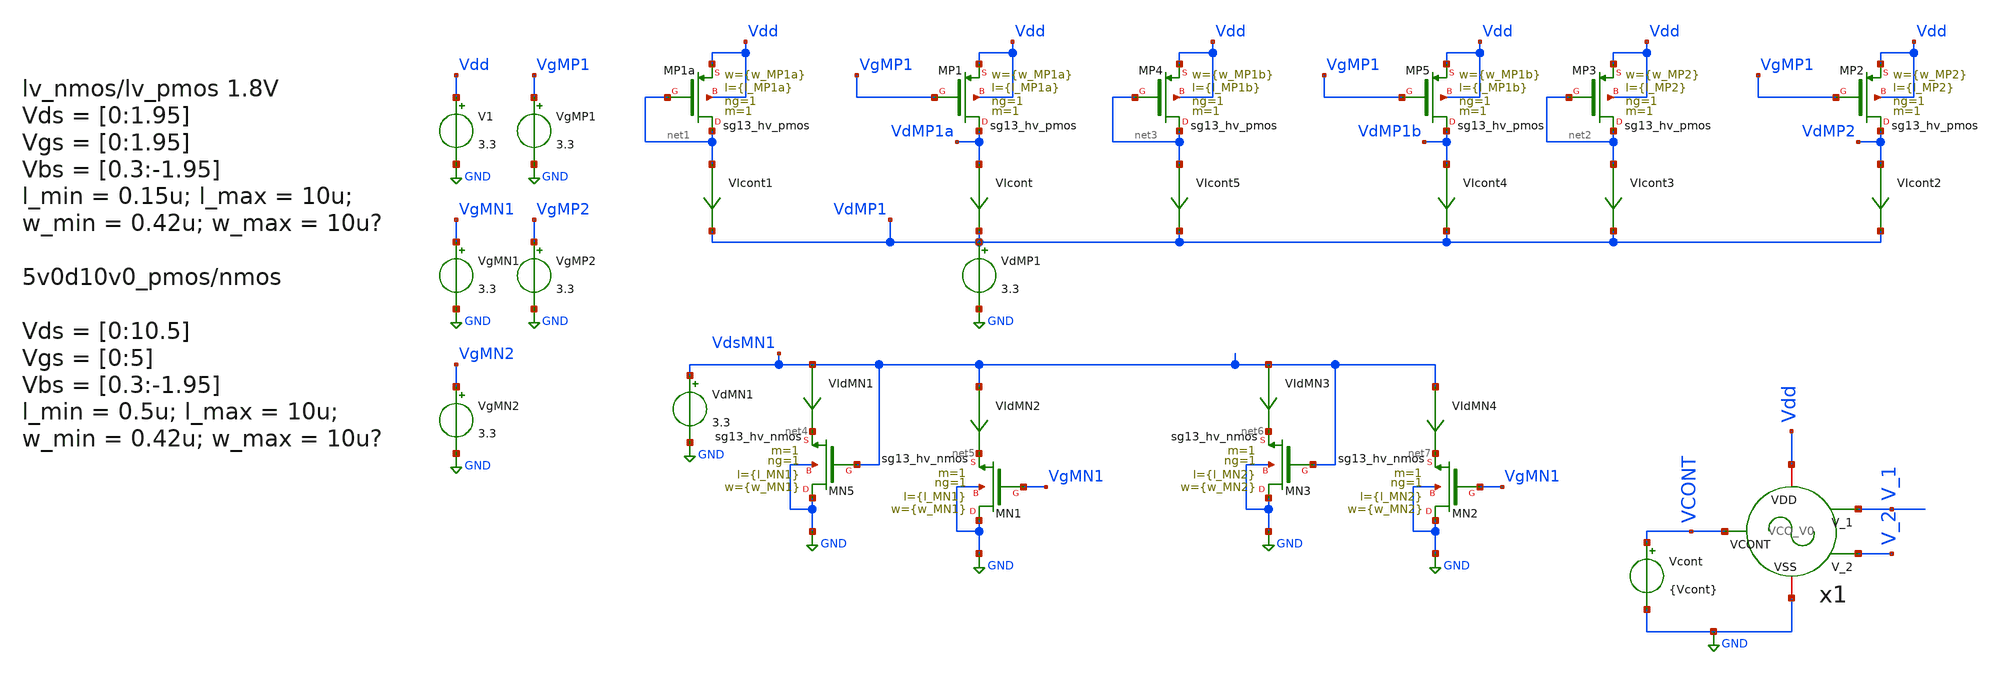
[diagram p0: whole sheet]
** sch_path: xschem/VCO/TB_VCO_Design_V0.sch
**.subckt TB_VCO_Design_V0
V1 Vdd GND 3.3
VIcont VdMP1a VdMP1 0
.save i(vicont)
VdMP1 VdMP1 GND 3.3
VgMP1 VgMP1 GND 3.3
VdMN1 VdsMN1 GND 3.3
VIdMN1 VdsMN1 net4 0
.save i(vidmn1)
VIcont1 net1 VdMP1 0
.save i(vicont1)
VIdMN2 VdsMN1 net5 0
.save i(vidmn2)
VgMN1 VgMN1 GND 3.3
VIdMN3 VdsMN1 net6 0
.save i(vidmn3)
VIdMN4 VdsMN1 net7 0
.save i(vidmn4)
VIcont2 VdMP2 VdMP1 0
.save i(vicont2)
VIcont3 net2 VdMP1 0
.save i(vicont3)
VgMP2 VgMP2 GND 3.3
VgMN2 VgMN2 GND 3.3
Vcont VCONT GND {Vcont}
x1 VCONT GND Vdd V_1 V_2 VCO_V0
XMP1a net1 net1 Vdd Vdd sg13_hv_pmos w={w_MP1a} l={l_MP1a} ng=1 m=1 mm_ok=1
XMP1 VdMP1a VgMP1 Vdd Vdd sg13_hv_pmos w={w_MP1a} l={l_MP1a} ng=1 m=1 mm_ok=1
XMP3 net2 net2 Vdd Vdd sg13_hv_pmos w={w_MP2} l={l_MP2} ng=1 m=1 mm_ok=1
XMP2 VdMP2 VgMP1 Vdd Vdd sg13_hv_pmos w={w_MP2} l={l_MP2} ng=1 m=1 mm_ok=1
XMN5 GND VdsMN1 net4 GND sg13_hv_nmos w={w_MN1} l={l_MN1} ng=1 m=1 mm_ok=1
XMN1 GND VgMN1 net5 GND sg13_hv_nmos w={w_MN1} l={l_MN1} ng=1 m=1 mm_ok=1
XMN3 GND VdsMN1 net6 GND sg13_hv_nmos w={w_MN2} l={l_MN2} ng=1 m=1 mm_ok=1
XMN2 GND VgMN1 net7 GND sg13_hv_nmos w={w_MN2} l={l_MN2} ng=1 m=1 mm_ok=1
VIcont4 VdMP1b VdMP1 0
.save i(vicont4)
VIcont5 net3 VdMP1 0
.save i(vicont5)
XMP4 net3 net3 Vdd Vdd sg13_hv_pmos w={w_MP1b} l={l_MP1b} ng=1 m=1 mm_ok=1
XMP5 VdMP1b VgMP1 Vdd Vdd sg13_hv_pmos w={w_MP1b} l={l_MP1b} ng=1 m=1 mm_ok=1
**** begin user architecture code


.save all


.csparam start = 10
.param Vcont = 1

.control

dc VdMP1 0 3.3 0.2 VgMP1 0 3.3 0.2
let IdMP1a = i(VIcont)
let IdMP1a_Diode = i(VIcont1)
let  VsdMP1 = v(Vdd) - v(VdMP1)
let VthMP1 = @n.xMP1.msky130_fd_pr__pfet_01v8[vth]
let  VovMP1a = v(Vdd) - v(VdMP1) - VthMP1
plot IdMP1a IdMP1a_Diode vs VsdMP1
plot IdMP1a_Diode vs VovMP1

let IdMP1b = i(VIcont4)
let IdMP1b_Diode = i(VIcont5)
let  VsdMP1 = v(Vdd) - v(VdMP1)
let VthMP1 = @n.xMP1.msky130_fd_pr__pfet_01v8[vth]
let  VovMP1b = v(Vdd) - v(VdMP1) - VthMP1
plot IdMP1b IdMP1b_Diode vs VsdMP1
plot IdMP1b_Diode vs VovMP1

let IdMP2 = i(VIcont2)
let IdMP2_Diode = i(VIcont3)
let  VsdMP2 = v(Vdd) - v(VdMP2)
let VthMP2 = @m.xMP4.msky130_fd_pr__pfet_01v8[vth]
let  VovMP2 = v(Vdd) - v(VdMP2) - VthMP2
*plot IdMP2 IdMP2_Diode vs VsdMP2
*plot IdMP2_Diode vs VovMP2
let KP1 = IdMP1_Diode/(VovMP1*VovMP1)
let AP1 = sqrt(KP1)
let KP2 = IdMP2_Diode/(VovMP2*VovMP2)
let AP2 = sqrt(KP2)

plot AP1 AP2

*plot IdMP1_Diode IdMP2_Diode vs VsdMP1
print VthMP1 VthMP2
*wrdata ../../sim_data/data_VCO_design.txt IdMP1_Diode VovMP1 IdMP1 vs VsdMP1
wrdata
+ /workspaces/usm-vlsi-tools/shared_xserver/simulations/SKY130/IPD500-TimebasedDCDCBuck/sim_data/data_VCO_design.txt IdMP1_Diode VovMP1 IdMP1 vs VsdMP1
wrdata
+ /workspaces/usm-vlsi-tools/shared_xserver/simulations/SKY130/IPD500-TimebasedDCDCBuck/sim_data/data_AP1_VthMP1.txt AP1 VthMP1 AP2 VthMP2

reset
*load save_data.raw
*show

dc VdMN1 0 3.3 0.2 VgMN1 0 3.3 0.2
let VdsMN1 = v(VdsMN1)
let IdMN1_Diode = i(VIdMN1)
let IdMN1 = i(VIdMN2)
let VthMN1 = @m.xMN1.msky130_fd_pr__nfet_01v8[vth]
let VovMN1 = VdsMN1 - VthMN1
plot IdMN1 IdMN1_Diode vs VdsMN1
plot IdMN1_Diode vs VovMN1

let VdsMN2 = v(VdsMN1)
let IdMN2_Diode = i(VIdMN3)
let IdMN2 = i(VIdMN4)
let VthMN2 = @m.xMN4.msky130_fd_pr__nfet_01v8[vth]
let VovMN2 = VdsMN2 - VthMN2
*plot IdMN2 IdMN2_Diode vs VdsMN2
*plot IdMN2_Diode vs VovMN2

let KN1 = IdMN1_Diode/(VovMN1*VovMN1)
let AN1 = sqrt(KN1)
let KN2 = IdMN2_Diode/(VovMN2*VovMN2)
let AN2 = sqrt(KN2)
plot AN1 AN2
print VthMN1 VthMN2
wrdata
+ /workspaces/usm-vlsi-tools/shared_xserver/simulations/SKY130/IPD500-TimebasedDCDCBuck/sim_data/data_AN1_VthMN1.txt AN1 VthMN1


reset

dc Vcont 0 2 0.1
let Icont = i(v.x1.x1.VIcont)
let Icont2 = i(v.x1.x1.VIcont1)
let VCN = v(x1.x1.VCN)
let VCP = v(x1.x1.VCP)


plot Icont Icont2 vs Vcont
*plot Iout vs VCP
plot VCP vs Vcont
plot VCN vs Vcont
*plot Vin vs Vcont
.endc

.control
reset
unset filetype
op
alter Vcont 1
write TB_VCO_design.raw
.endc





.lib cornerMOShv.lib mos_tt
.lib cornerMOSlv.lib mos_tt
*.lib cornerMOShv.lib mos_ff
*.lib cornerMOSlv.lib mos_ff
*.lib cornerMOShv.lib mos_ss
*.lib cornerMOSlv.lib mos_ss
*.lib cornerMOShv.lib mos_sf
*.lib cornerMOSlv.lib mos_sf
*.lib cornerMOShv.lib mos_fs
*.lib cornerMOSlv.lib mos_fs

*.include /opt/pdks/ihp-sg13g2/libs.ref/sg13g2_stdcell/spice/sg13g2_stdcell.spice
*.lib $::SG13G2_MODELS/cornerRES.lib res_typ
*.lib $::SG13G2_MODELS/cornerCAP.lib cap_typ
*.lib $::SG13G2_MODELS/diodes.lib



.param Vcont2 = 1.8

.param w_MP1a = 2u
.param l_MP1a = 7u
.param w_MP1b = 3u
.param l_MP1b = 7u
.param w_MP2 = 8u
.param l_MP2 = 4u
.param w_MP3 = 5u
.param l_MP3 = 4u
.param w_MP4 = 5u
.param l_MP4 = 5u

.param w_MN1 = 5u
.param l_MN1 = 0.5u
.param w_MN2 = 5u
.param l_MN2 = 0.5u
.param w_MN3 = 3u
.param l_MN3 = 0.5u
.param w_MN4 = 2u
.param l_MN4 = 5u




**** end user architecture code
**.ends
.GLOBAL GND
.end
